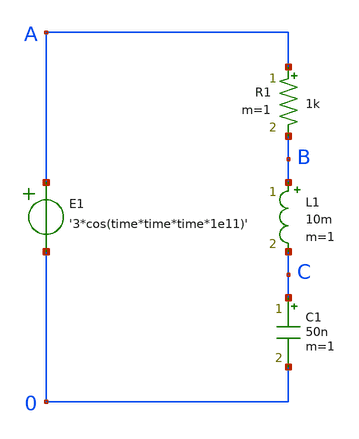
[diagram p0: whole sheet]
** sch_path: 2_Ideal_Cir/RLC_test.sch
**.subckt RLC_test
C1 C 0 50n m=1
L1 B C 10m m=1
R1 A B 1k m=1
E1 A 0 VOL=' '3*cos(time*time*time*1e11)' '
**** begin user architecture code

.tran 10n 2000u uic .save all

**** end user architecture code
**.ends
.end
